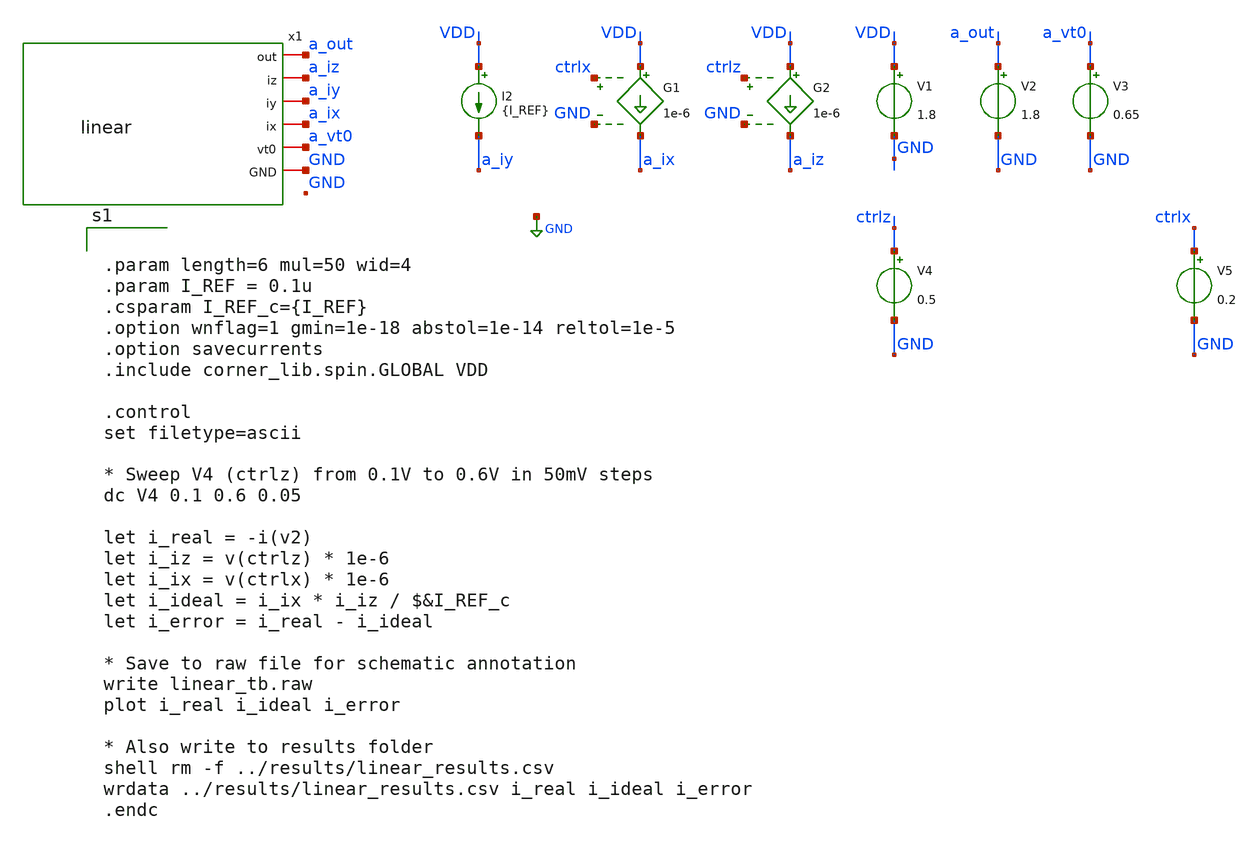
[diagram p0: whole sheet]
** sch_path: xschem/archive/old_blocks/linear_tb.sch
**.subckt linear_tb
I2 VDD a_iy {I_REF}
G1 VDD a_ix ctrlx GND 1e-6
G2 VDD a_iz ctrlz GND 1e-6
V1 VDD GND 1.8
V2 a_out GND 1.8
V3 a_vt0 GND 0.65
V4 ctrlz GND 0.5
x1 a_out a_iz a_iy a_ix a_vt0 GND linear
V5 ctrlx GND 0.2
**** begin user architecture code


.param length=6 mul=50 wid=4
.param I_REF = 0.1u
.csparam I_REF_c={I_REF}
.option wnflag=1 gmin=1e-18 abstol=1e-14 reltol=1e-5
.option savecurrents
.include corner_lib.spin.GLOBAL VDD

.control
set filetype=ascii

* Sweep V4 (ctrlz) from 0.1V to 0.6V in 50mV steps
dc V4 0.1 0.6 0.05

let i_real = -i(v2)
let i_iz = v(ctrlz) * 1e-6
let i_ix = v(ctrlx) * 1e-6
let i_ideal = i_ix * i_iz / $&I_REF_c
let i_error = i_real - i_ideal

* Save to raw file for schematic annotation
write linear_tb.raw
plot i_real i_ideal i_error

* Also write to results folder
shell rm -f ../results/linear_results.csv
wrdata ../results/linear_results.csv i_real i_ideal i_error
.endc


**** end user architecture code
**.ends

* expanding   symbol:  archive/old_blocks/linear.sym # of pins=6
** sym_path: xschem/archive/old_blocks/linear.sym
** sch_path: xschem/archive/old_blocks/linear.sch
.subckt linear out iz iy ix vt0 GND
*.iopin vt0
*.iopin ix
*.iopin iy
*.iopin iz
*.iopin out
*.iopin GND
XM18 net1 ix GND GND sky130_fd_pr__nfet_01v8 L=4 W=1.2 nf=1 ad='int((nf+1)/2) * W/nf * 0.29' as='int((nf+2)/2) * W/nf * 0.29'
+ pd='2*int((nf+1)/2) * (W/nf + 0.29)' ps='2*int((nf+2)/2) * (W/nf + 0.29)' nrd='0.29 / W' nrs='0.29 / W'
+ sa=0 sb=0 sd=0 mult=1 m=1
XM1 ix vt0 net1 GND sky130_fd_pr__nfet_01v8 L=length W=wid nf=1 ad='int((nf+1)/2) * W/nf * 0.29' as='int((nf+2)/2) * W/nf * 0.29'
+ pd='2*int((nf+1)/2) * (W/nf + 0.29)' ps='2*int((nf+2)/2) * (W/nf + 0.29)' nrd='0.29 / W' nrs='0.29 / W'
+ sa=0 sb=0 sd=0 mult=mul m=mul
XM2 net2 iz GND GND sky130_fd_pr__nfet_01v8 L=4 W=1.2 nf=1 ad='int((nf+1)/2) * W/nf * 0.29' as='int((nf+2)/2) * W/nf * 0.29'
+ pd='2*int((nf+1)/2) * (W/nf + 0.29)' ps='2*int((nf+2)/2) * (W/nf + 0.29)' nrd='0.29 / W' nrs='0.29 / W'
+ sa=0 sb=0 sd=0 mult=1 m=1
XM3 iz iy net2 GND sky130_fd_pr__nfet_01v8 L=length W=wid nf=1 ad='int((nf+1)/2) * W/nf * 0.29' as='int((nf+2)/2) * W/nf * 0.29'
+ pd='2*int((nf+1)/2) * (W/nf + 0.29)' ps='2*int((nf+2)/2) * (W/nf + 0.29)' nrd='0.29 / W' nrs='0.29 / W'
+ sa=0 sb=0 sd=0 mult=mul m=mul
XM4 iy iy net1 GND sky130_fd_pr__nfet_01v8 L=length W=wid nf=1 ad='int((nf+1)/2) * W/nf * 0.29' as='int((nf+2)/2) * W/nf * 0.29'
+ pd='2*int((nf+1)/2) * (W/nf + 0.29)' ps='2*int((nf+2)/2) * (W/nf + 0.29)' nrd='0.29 / W' nrs='0.29 / W'
+ sa=0 sb=0 sd=0 mult=mul m=mul
XM5 net3 vt0 net2 GND sky130_fd_pr__nfet_01v8 L=length W=wid nf=1 ad='int((nf+1)/2) * W/nf * 0.29' as='int((nf+2)/2) * W/nf * 0.29'
+ pd='2*int((nf+1)/2) * (W/nf + 0.29)' ps='2*int((nf+2)/2) * (W/nf + 0.29)' nrd='0.29 / W' nrs='0.29 / W'
+ sa=0 sb=0 sd=0 mult=mul m=mul
XM26 net3 net3 out VDD sky130_fd_pr__pfet_01v8 L=length W=wid/2 nf=1 ad='int((1 + 1)/2) * wid/2 / 1 * 0.29'
+ as='int((1 + 2)/2) * wid/2 / 1 * 0.29' pd='2*int((1 + 1)/2) * (wid/2 / 1 + 0.29)' ps='2*int((1 + 2)/2) * (wid/2 / 1 + 0.29)'
+ nrd='0.29 / wid/2 ' nrs='0.29 / wid/2 ' sa=0 sb=0 sd=0 mult=mul m=mul
.ends

.GLOBAL GND
.end
